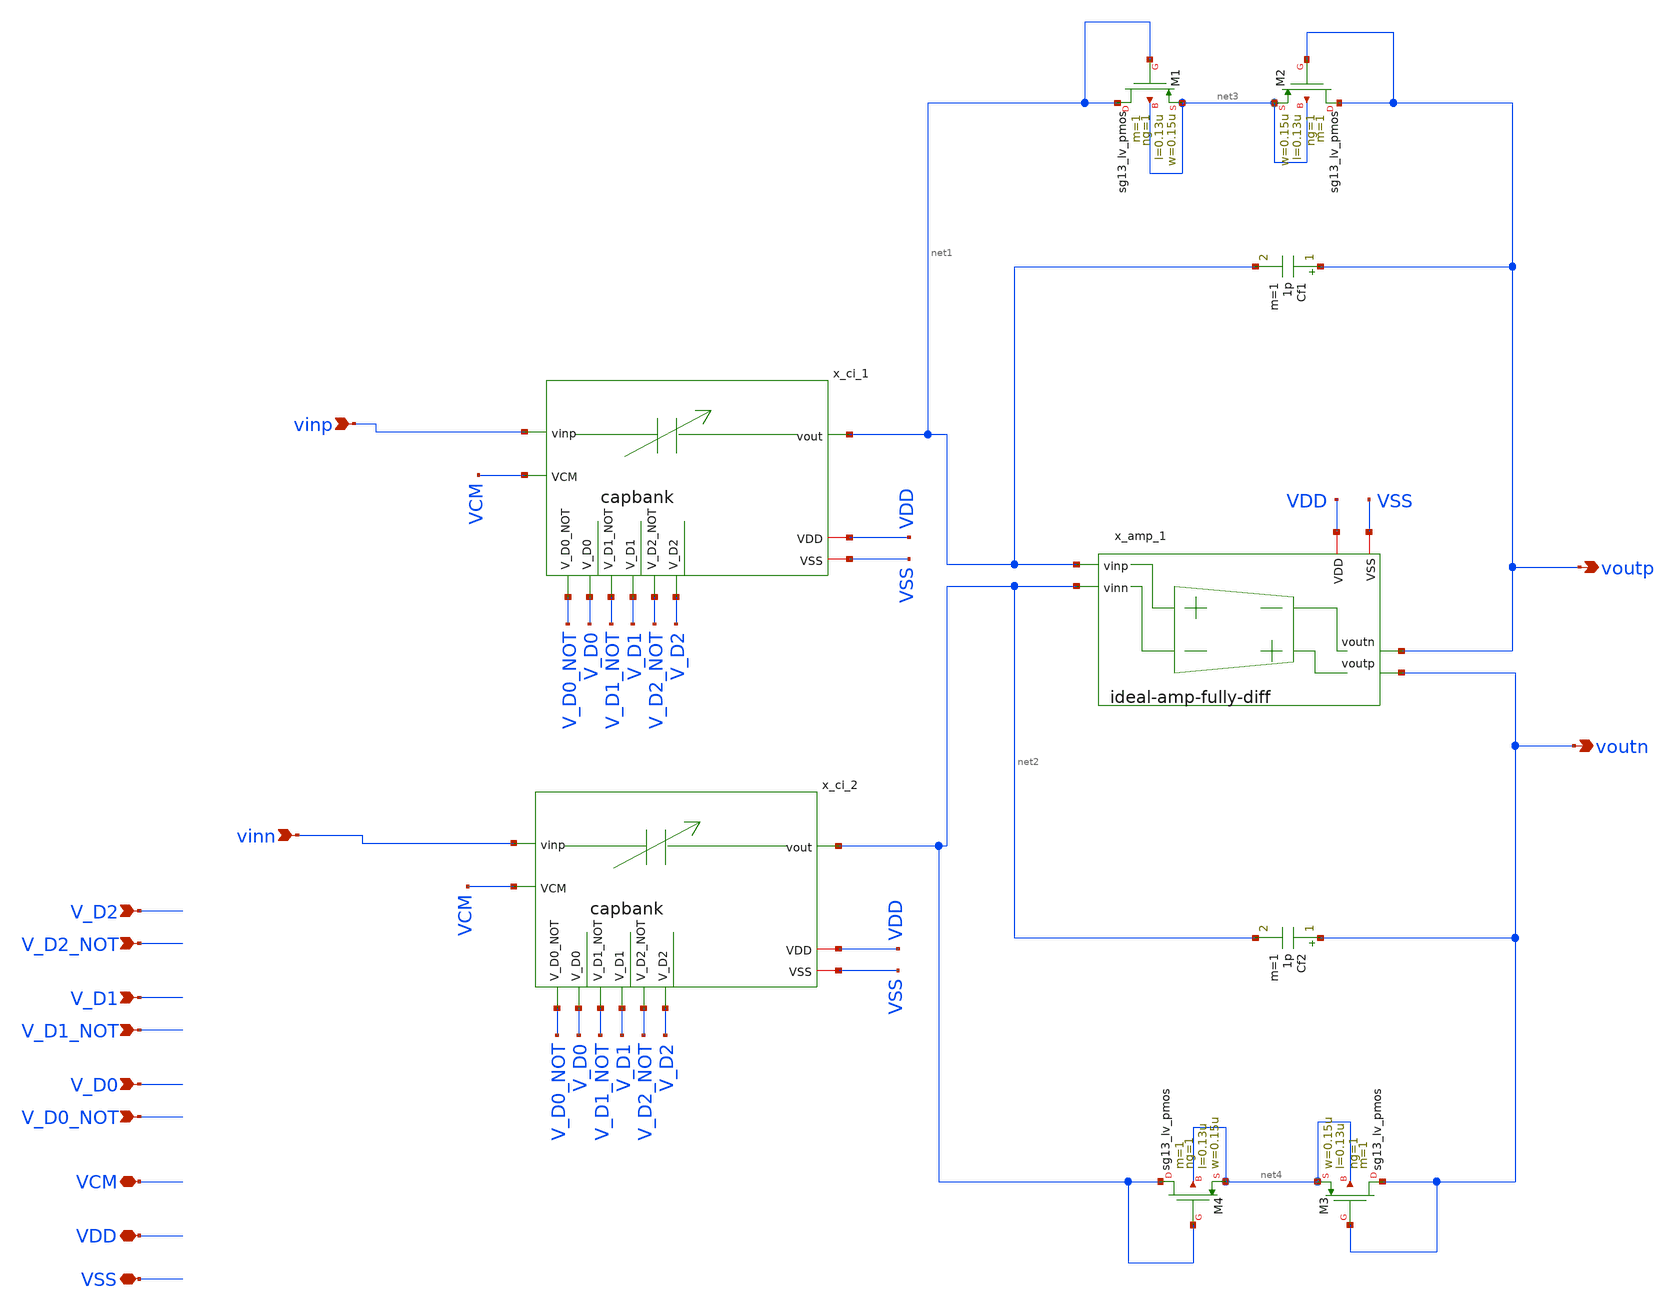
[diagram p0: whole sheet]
** sch_path: analog-db/circuits/ia_005_hsu_pga_ideal/pdk/ihp-sg13g2/schematic/PGA-ideal.sch
* Copyright 2026 MacAnalog Research Group
**.subckt PGA-ideal VDD VSS V_D0 V_D0_NOT V_D1 V_D1_NOT V_D2 V_D2_NOT vinn vinp voutp voutn VCM
*.iopin VDD
*.iopin VSS
*.ipin V_D0
*.ipin V_D0_NOT
*.ipin V_D1
*.ipin V_D1_NOT
*.ipin V_D2
*.ipin V_D2_NOT
*.ipin vinn
*.ipin vinp
*.opin voutp
*.opin voutn
*.iopin VCM
x_amp_1 net1 net2 voutp voutn VSS VDD ideal-amp-fully-diff
x_ci_1 vinp net1 VCM VDD VSS V_D0 V_D0_NOT V_D1 V_D1_NOT V_D2 V_D2_NOT capbank
x_ci_2 vinn net2 VCM VDD VSS V_D0 V_D0_NOT V_D1 V_D1_NOT V_D2 V_D2_NOT capbank
Cf1 voutp net1 1p m=1
Cf2 voutn net2 1p m=1
XM2 voutp voutp net3 net3 sg13_lv_pmos w=0.15u l=0.13u ng=1 m=1 mm_ok=1
XM1 net1 net1 net3 net3 sg13_lv_pmos w=0.15u l=0.13u ng=1 m=1 mm_ok=1
XM3 voutn voutn net4 net4 sg13_lv_pmos w=0.15u l=0.13u ng=1 m=1 mm_ok=1
XM4 net2 net2 net4 net4 sg13_lv_pmos w=0.15u l=0.13u ng=1 m=1 mm_ok=1
**.ends
.end
